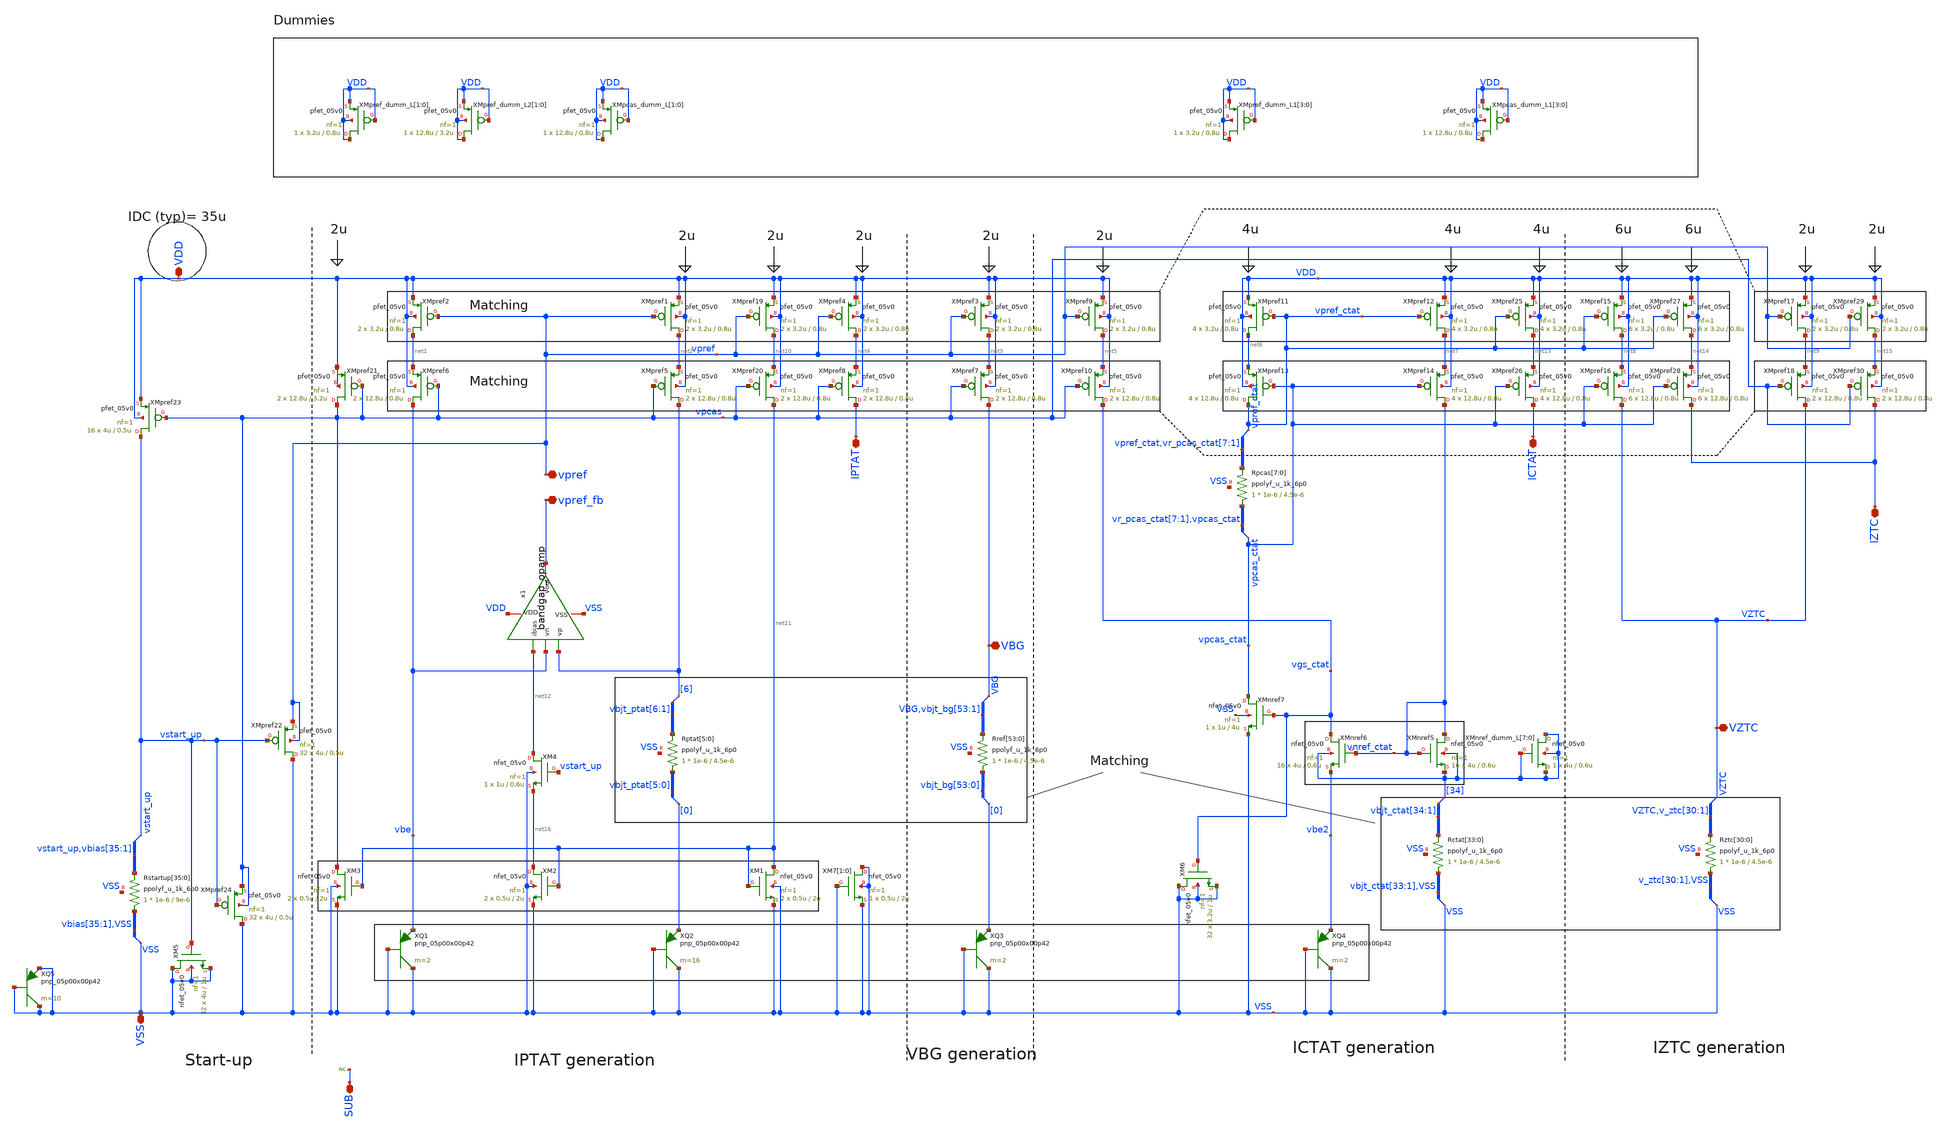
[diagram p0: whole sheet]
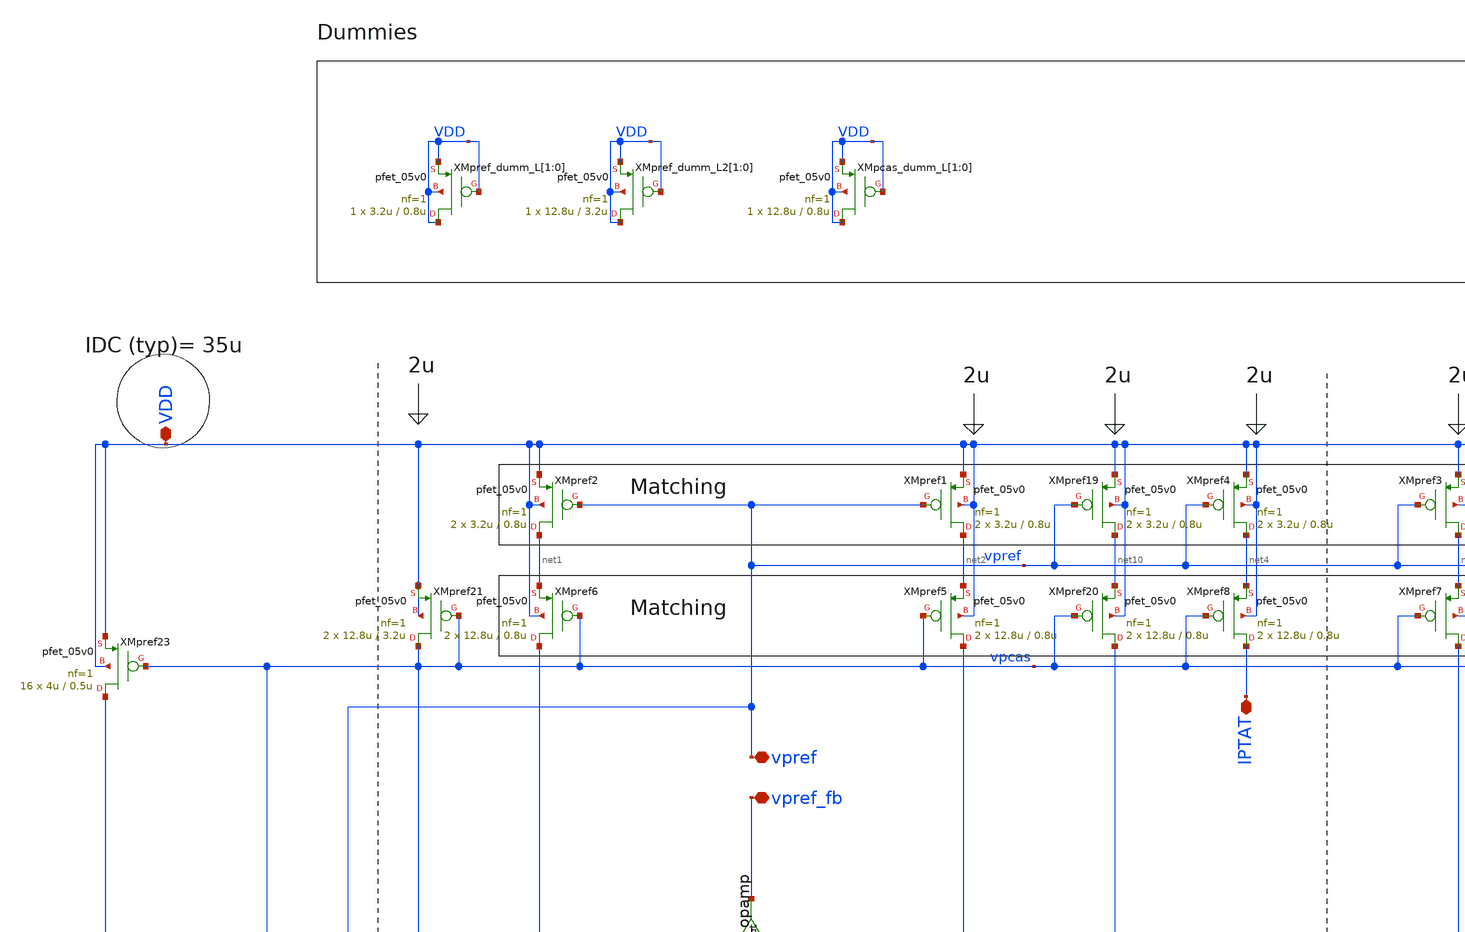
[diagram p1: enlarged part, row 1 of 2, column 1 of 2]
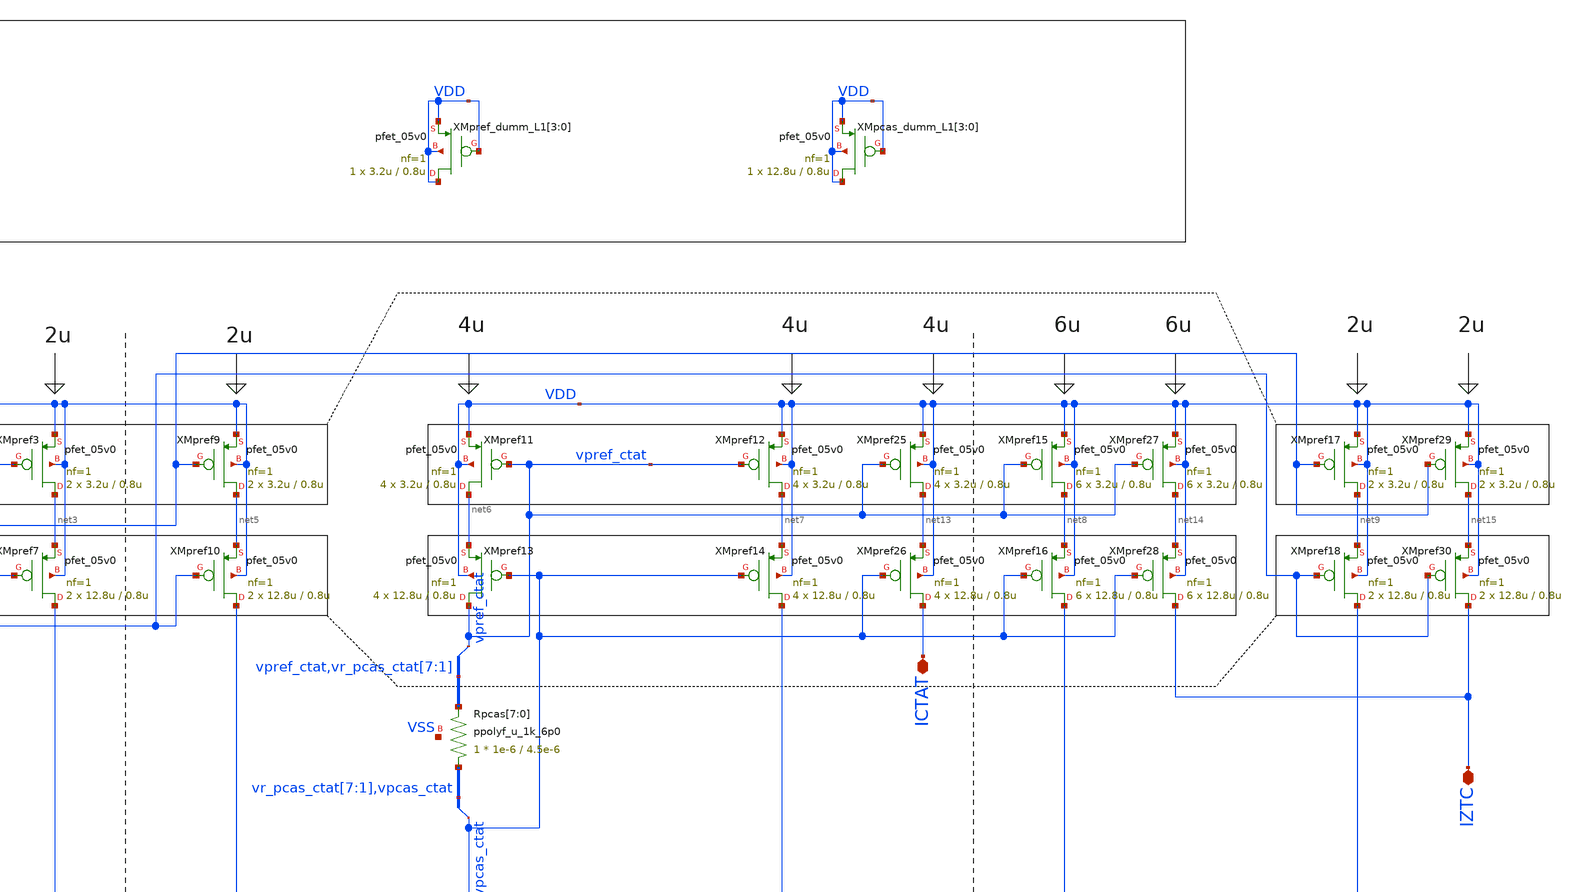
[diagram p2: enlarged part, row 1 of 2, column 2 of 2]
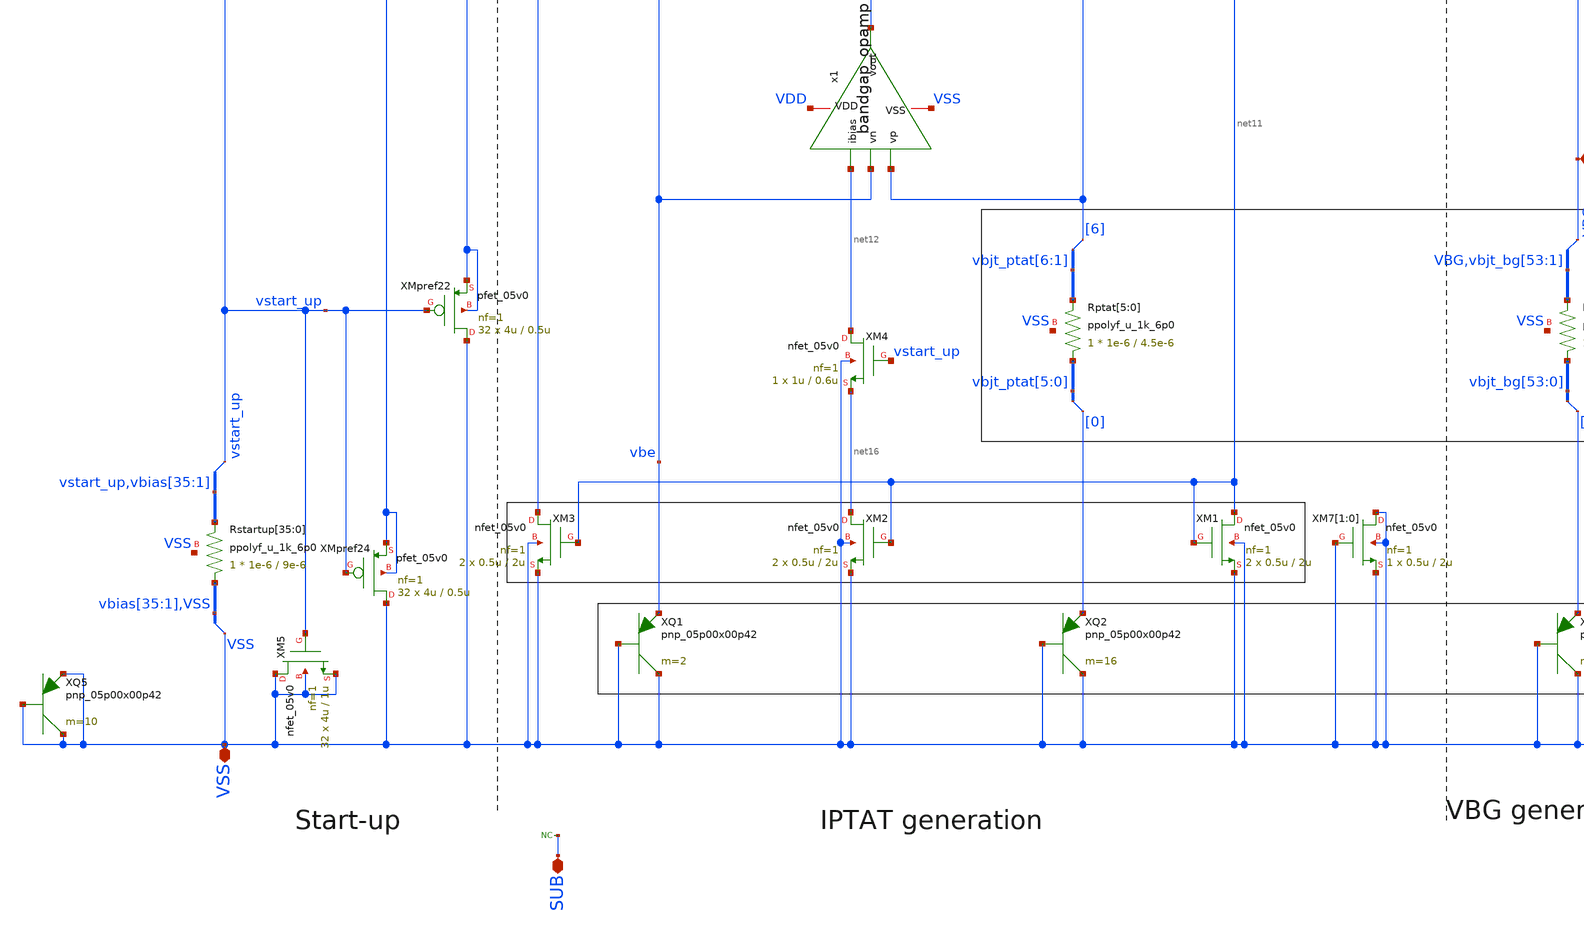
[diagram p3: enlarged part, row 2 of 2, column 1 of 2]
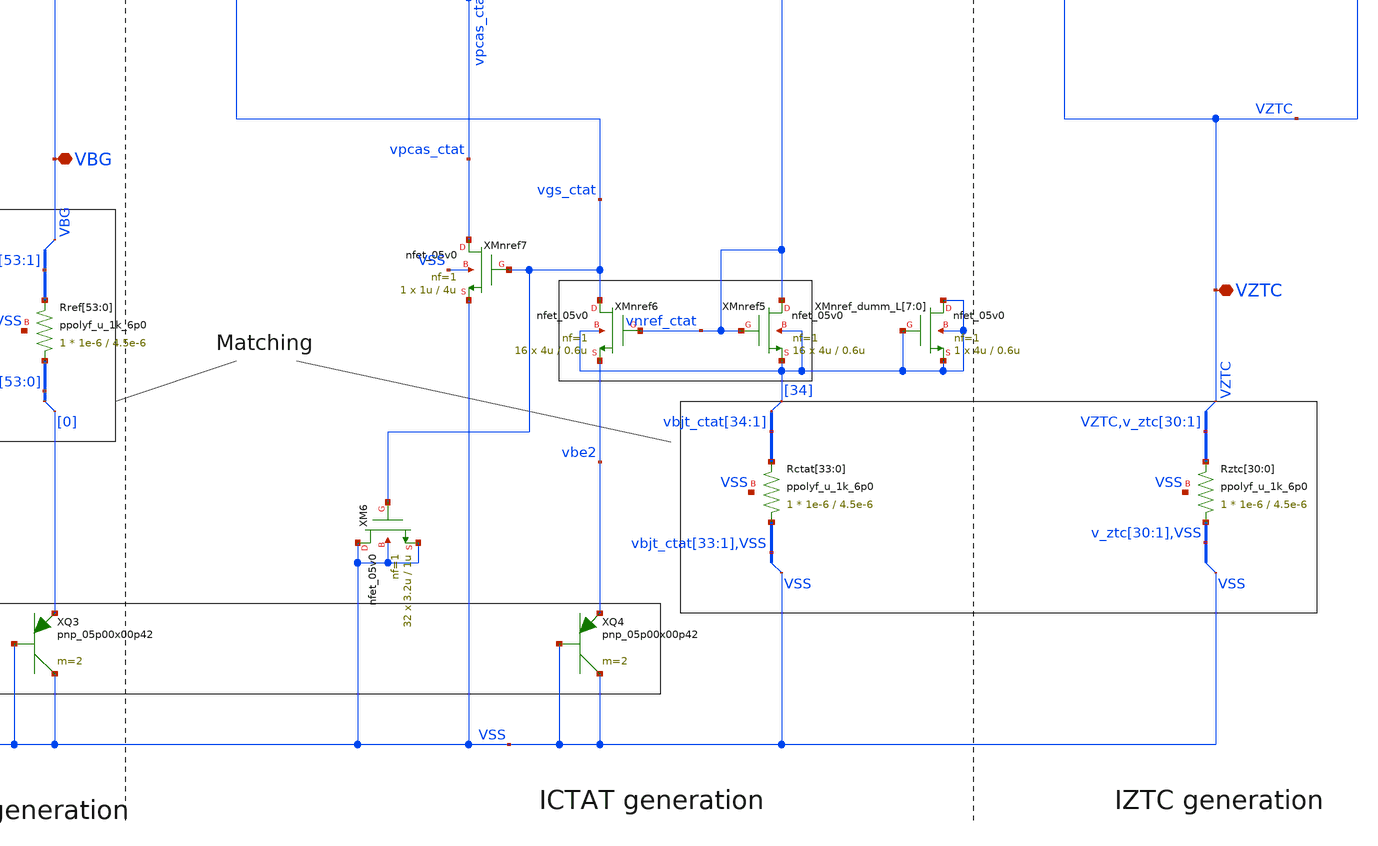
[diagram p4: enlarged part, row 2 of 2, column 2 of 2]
** sch_path: designs/libs/core_bandgap/bandgap/bandgap.sch
**.subckt bandgap VDD VSS SUB VBG IPTAT IZTC vpref vpref_fb ICTAT VZTC
*.iopin VDD
*.iopin VSS
*.iopin SUB
*.iopin VBG
*.iopin IPTAT
*.iopin IZTC
*.iopin vpref
*.iopin vpref_fb
*.iopin ICTAT
*.iopin VZTC
* noconn SUB
XMpref1 net2 vpref VDD VDD pfet_05v0 L=0.8u W=3.2u nf=1 ad='int((nf+1)/2) * W/nf * 0.18u' as='int((nf+2)/2) * W/nf * 0.18u'
+ pd='2*int((nf+1)/2) * (W/nf + 0.18u)' ps='2*int((nf+2)/2) * (W/nf + 0.18u)' nrd='0.18u / W' nrs='0.18u / W'
+ sa=0 sb=0 sd=0 m=2
XMpref2 net1 vpref VDD VDD pfet_05v0 L=0.8u W=3.2u nf=1 ad='int((nf+1)/2) * W/nf * 0.18u' as='int((nf+2)/2) * W/nf * 0.18u'
+ pd='2*int((nf+1)/2) * (W/nf + 0.18u)' ps='2*int((nf+2)/2) * (W/nf + 0.18u)' nrd='0.18u / W' nrs='0.18u / W'
+ sa=0 sb=0 sd=0 m=2
* tap: vbjt_ptat[5:0] --> vbjt_ptat[0]
* tap: vbjt_ptat[6:1] --> vbjt_ptat[6]
XMpref3 net3 vpref VDD VDD pfet_05v0 L=0.8u W=3.2u nf=1 ad='int((nf+1)/2) * W/nf * 0.18u' as='int((nf+2)/2) * W/nf * 0.18u'
+ pd='2*int((nf+1)/2) * (W/nf + 0.18u)' ps='2*int((nf+2)/2) * (W/nf + 0.18u)' nrd='0.18u / W' nrs='0.18u / W'
+ sa=0 sb=0 sd=0 m=2
* tap: vbjt_bg[53:0] --> vbjt_bg[0]
XMpref4 net4 vpref VDD VDD pfet_05v0 L=0.8u W=3.2u nf=1 ad='int((nf+1)/2) * W/nf * 0.18u' as='int((nf+2)/2) * W/nf * 0.18u'
+ pd='2*int((nf+1)/2) * (W/nf + 0.18u)' ps='2*int((nf+2)/2) * (W/nf + 0.18u)' nrd='0.18u / W' nrs='0.18u / W'
+ sa=0 sb=0 sd=0 m=2
XMpref5 vbjt_ptat[6] vpcas net2 VDD pfet_05v0 L=0.8u W=12.8u nf=1 ad='int((nf+1)/2) * W/nf * 0.18u' as='int((nf+2)/2) * W/nf * 0.18u'
+ pd='2*int((nf+1)/2) * (W/nf + 0.18u)' ps='2*int((nf+2)/2) * (W/nf + 0.18u)' nrd='0.18u / W' nrs='0.18u / W'
+ sa=0 sb=0 sd=0 m=2
XMpref6 vbe vpcas net1 VDD pfet_05v0 L=0.8u W=12.8u nf=1 ad='int((nf+1)/2) * W/nf * 0.18u' as='int((nf+2)/2) * W/nf * 0.18u'
+ pd='2*int((nf+1)/2) * (W/nf + 0.18u)' ps='2*int((nf+2)/2) * (W/nf + 0.18u)' nrd='0.18u / W' nrs='0.18u / W'
+ sa=0 sb=0 sd=0 m=2
XMpref7 VBG vpcas net3 VDD pfet_05v0 L=0.8u W=12.8u nf=1 ad='int((nf+1)/2) * W/nf * 0.18u' as='int((nf+2)/2) * W/nf * 0.18u'
+ pd='2*int((nf+1)/2) * (W/nf + 0.18u)' ps='2*int((nf+2)/2) * (W/nf + 0.18u)' nrd='0.18u / W' nrs='0.18u / W'
+ sa=0 sb=0 sd=0 m=2
XMpref8 IPTAT vpcas net4 VDD pfet_05v0 L=0.8u W=12.8u nf=1 ad='int((nf+1)/2) * W/nf * 0.18u' as='int((nf+2)/2) * W/nf * 0.18u'
+ pd='2*int((nf+1)/2) * (W/nf + 0.18u)' ps='2*int((nf+2)/2) * (W/nf + 0.18u)' nrd='0.18u / W' nrs='0.18u / W'
+ sa=0 sb=0 sd=0 m=2
XMnref5 vnref_ctat vnref_ctat vbjt_ctat[34] vbjt_ctat[34] nfet_05v0 L=0.6u W=4u nf=1 ad='int((nf+1)/2) * W/nf * 0.18u'
+ as='int((nf+2)/2) * W/nf * 0.18u' pd='2*int((nf+1)/2) * (W/nf + 0.18u)' ps='2*int((nf+2)/2) * (W/nf + 0.18u)'
+ nrd='0.18u / W' nrs='0.18u / W' sa=0 sb=0 sd=0 m=16
XMnref6 vgs_ctat vnref_ctat vbe2 vbjt_ctat[34] nfet_05v0 L=0.6u W=4u nf=1 ad='int((nf+1)/2) * W/nf * 0.18u'
+ as='int((nf+2)/2) * W/nf * 0.18u' pd='2*int((nf+1)/2) * (W/nf + 0.18u)' ps='2*int((nf+2)/2) * (W/nf + 0.18u)'
+ nrd='0.18u / W' nrs='0.18u / W' sa=0 sb=0 sd=0 m=16
* tap: vbjt_ctat[34:1] --> vbjt_ctat[34]
XMnref7 vpcas_ctat vgs_ctat VSS VSS nfet_05v0 L=4u W=1u nf=1 ad='int((nf+1)/2) * W/nf * 0.18u' as='int((nf+2)/2) * W/nf * 0.18u'
+ pd='2*int((nf+1)/2) * (W/nf + 0.18u)' ps='2*int((nf+2)/2) * (W/nf + 0.18u)' nrd='0.18u / W' nrs='0.18u / W'
+ sa=0 sb=0 sd=0 m=1
XMpref9 net5 vpref VDD VDD pfet_05v0 L=0.8u W=3.2u nf=1 ad='int((nf+1)/2) * W/nf * 0.18u' as='int((nf+2)/2) * W/nf * 0.18u'
+ pd='2*int((nf+1)/2) * (W/nf + 0.18u)' ps='2*int((nf+2)/2) * (W/nf + 0.18u)' nrd='0.18u / W' nrs='0.18u / W'
+ sa=0 sb=0 sd=0 m=2
XMpref10 vgs_ctat vpcas net5 VDD pfet_05v0 L=0.8u W=12.8u nf=1 ad='int((nf+1)/2) * W/nf * 0.18u' as='int((nf+2)/2) * W/nf * 0.18u'
+ pd='2*int((nf+1)/2) * (W/nf + 0.18u)' ps='2*int((nf+2)/2) * (W/nf + 0.18u)' nrd='0.18u / W' nrs='0.18u / W'
+ sa=0 sb=0 sd=0 m=2
XMpref11 net6 vpref_ctat VDD VDD pfet_05v0 L=0.8u W=3.2u nf=1 ad='int((nf+1)/2) * W/nf * 0.18u' as='int((nf+2)/2) * W/nf * 0.18u'
+ pd='2*int((nf+1)/2) * (W/nf + 0.18u)' ps='2*int((nf+2)/2) * (W/nf + 0.18u)' nrd='0.18u / W' nrs='0.18u / W'
+ sa=0 sb=0 sd=0 m=4
XMpref12 net7 vpref_ctat VDD VDD pfet_05v0 L=0.8u W=3.2u nf=1 ad='int((nf+1)/2) * W/nf * 0.18u' as='int((nf+2)/2) * W/nf * 0.18u'
+ pd='2*int((nf+1)/2) * (W/nf + 0.18u)' ps='2*int((nf+2)/2) * (W/nf + 0.18u)' nrd='0.18u / W' nrs='0.18u / W'
+ sa=0 sb=0 sd=0 m=4
XMpref13 vpref_ctat vpcas_ctat net6 VDD pfet_05v0 L=0.8u W=12.8u nf=1 ad='int((nf+1)/2) * W/nf * 0.18u'
+ as='int((nf+2)/2) * W/nf * 0.18u' pd='2*int((nf+1)/2) * (W/nf + 0.18u)' ps='2*int((nf+2)/2) * (W/nf + 0.18u)'
+ nrd='0.18u / W' nrs='0.18u / W' sa=0 sb=0 sd=0 m=4
XMpref14 vnref_ctat vpcas_ctat net7 VDD pfet_05v0 L=0.8u W=12.8u nf=1 ad='int((nf+1)/2) * W/nf * 0.18u'
+ as='int((nf+2)/2) * W/nf * 0.18u' pd='2*int((nf+1)/2) * (W/nf + 0.18u)' ps='2*int((nf+2)/2) * (W/nf + 0.18u)'
+ nrd='0.18u / W' nrs='0.18u / W' sa=0 sb=0 sd=0 m=4
XMpref15 net8 vpref_ctat VDD VDD pfet_05v0 L=0.8u W=3.2u nf=1 ad='int((nf+1)/2) * W/nf * 0.18u' as='int((nf+2)/2) * W/nf * 0.18u'
+ pd='2*int((nf+1)/2) * (W/nf + 0.18u)' ps='2*int((nf+2)/2) * (W/nf + 0.18u)' nrd='0.18u / W' nrs='0.18u / W'
+ sa=0 sb=0 sd=0 m=6
XMpref16 VZTC vpcas_ctat net8 VDD pfet_05v0 L=0.8u W=12.8u nf=1 ad='int((nf+1)/2) * W/nf * 0.18u' as='int((nf+2)/2) * W/nf * 0.18u'
+ pd='2*int((nf+1)/2) * (W/nf + 0.18u)' ps='2*int((nf+2)/2) * (W/nf + 0.18u)' nrd='0.18u / W' nrs='0.18u / W'
+ sa=0 sb=0 sd=0 m=6
XMpref17 net9 vpref VDD VDD pfet_05v0 L=0.8u W=3.2u nf=1 ad='int((nf+1)/2) * W/nf * 0.18u' as='int((nf+2)/2) * W/nf * 0.18u'
+ pd='2*int((nf+1)/2) * (W/nf + 0.18u)' ps='2*int((nf+2)/2) * (W/nf + 0.18u)' nrd='0.18u / W' nrs='0.18u / W'
+ sa=0 sb=0 sd=0 m=2
XMpref18 VZTC vpcas net9 VDD pfet_05v0 L=0.8u W=12.8u nf=1 ad='int((nf+1)/2) * W/nf * 0.18u' as='int((nf+2)/2) * W/nf * 0.18u'
+ pd='2*int((nf+1)/2) * (W/nf + 0.18u)' ps='2*int((nf+2)/2) * (W/nf + 0.18u)' nrd='0.18u / W' nrs='0.18u / W'
+ sa=0 sb=0 sd=0 m=2
XMpref_dumm_L[1] VDD VDD VDD VDD pfet_05v0 L=0.8u W=3.2u nf=1 ad='int((nf+1)/2) * W/nf * 0.18u' as='int((nf+2)/2) * W/nf * 0.18u'
+ pd='2*int((nf+1)/2) * (W/nf + 0.18u)' ps='2*int((nf+2)/2) * (W/nf + 0.18u)' nrd='0.18u / W' nrs='0.18u / W'
+ sa=0 sb=0 sd=0 m=1
XMpref_dumm_L[0] VDD VDD VDD VDD pfet_05v0 L=0.8u W=3.2u nf=1 ad='int((nf+1)/2) * W/nf * 0.18u' as='int((nf+2)/2) * W/nf * 0.18u'
+ pd='2*int((nf+1)/2) * (W/nf + 0.18u)' ps='2*int((nf+2)/2) * (W/nf + 0.18u)' nrd='0.18u / W' nrs='0.18u / W'
+ sa=0 sb=0 sd=0 m=1
x1 VDD net12 vbe vbjt_ptat[6] vpref_fb VSS bandgap_opamp
XMpref19 net10 vpref VDD VDD pfet_05v0 L=0.8u W=3.2u nf=1 ad='int((nf+1)/2) * W/nf * 0.18u' as='int((nf+2)/2) * W/nf * 0.18u'
+ pd='2*int((nf+1)/2) * (W/nf + 0.18u)' ps='2*int((nf+2)/2) * (W/nf + 0.18u)' nrd='0.18u / W' nrs='0.18u / W'
+ sa=0 sb=0 sd=0 m=2
XMpref20 net11 vpcas net10 VDD pfet_05v0 L=0.8u W=12.8u nf=1 ad='int((nf+1)/2) * W/nf * 0.18u' as='int((nf+2)/2) * W/nf * 0.18u'
+ pd='2*int((nf+1)/2) * (W/nf + 0.18u)' ps='2*int((nf+2)/2) * (W/nf + 0.18u)' nrd='0.18u / W' nrs='0.18u / W'
+ sa=0 sb=0 sd=0 m=2
XM1 net11 net11 VSS VSS nfet_05v0 L=2u W=0.5u nf=1 ad='int((nf+1)/2) * W/nf * 0.18u' as='int((nf+2)/2) * W/nf * 0.18u'
+ pd='2*int((nf+1)/2) * (W/nf + 0.18u)' ps='2*int((nf+2)/2) * (W/nf + 0.18u)' nrd='0.18u / W' nrs='0.18u / W'
+ sa=0 sb=0 sd=0 m=2
XM2 net16 net11 VSS VSS nfet_05v0 L=2u W=0.5u nf=1 ad='int((nf+1)/2) * W/nf * 0.18u' as='int((nf+2)/2) * W/nf * 0.18u'
+ pd='2*int((nf+1)/2) * (W/nf + 0.18u)' ps='2*int((nf+2)/2) * (W/nf + 0.18u)' nrd='0.18u / W' nrs='0.18u / W'
+ sa=0 sb=0 sd=0 m=2
XM3 vpcas net11 VSS VSS nfet_05v0 L=2u W=0.5u nf=1 ad='int((nf+1)/2) * W/nf * 0.18u' as='int((nf+2)/2) * W/nf * 0.18u'
+ pd='2*int((nf+1)/2) * (W/nf + 0.18u)' ps='2*int((nf+2)/2) * (W/nf + 0.18u)' nrd='0.18u / W' nrs='0.18u / W'
+ sa=0 sb=0 sd=0 m=2
XMpref21 vpcas vpcas VDD VDD pfet_05v0 L=3.2u W=12.8u nf=1 ad='int((nf+1)/2) * W/nf * 0.18u' as='int((nf+2)/2) * W/nf * 0.18u'
+ pd='2*int((nf+1)/2) * (W/nf + 0.18u)' ps='2*int((nf+2)/2) * (W/nf + 0.18u)' nrd='0.18u / W' nrs='0.18u / W'
+ sa=0 sb=0 sd=0 m=2
XMpref23 vstart_up vpcas VDD VDD pfet_05v0 L=0.5u W=4u nf=1 ad='int((nf+1)/2) * W/nf * 0.18u' as='int((nf+2)/2) * W/nf * 0.18u'
+ pd='2*int((nf+1)/2) * (W/nf + 0.18u)' ps='2*int((nf+2)/2) * (W/nf + 0.18u)' nrd='0.18u / W' nrs='0.18u / W'
+ sa=0 sb=0 sd=0 m=16
XMpref24 VSS vstart_up vpcas vpcas pfet_05v0 L=0.5u W=4u nf=1 ad='int((nf+1)/2) * W/nf * 0.18u' as='int((nf+2)/2) * W/nf * 0.18u'
+ pd='2*int((nf+1)/2) * (W/nf + 0.18u)' ps='2*int((nf+2)/2) * (W/nf + 0.18u)' nrd='0.18u / W' nrs='0.18u / W'
+ sa=0 sb=0 sd=0 m=32
XMpref25 net13 vpref_ctat VDD VDD pfet_05v0 L=0.8u W=3.2u nf=1 ad='int((nf+1)/2) * W/nf * 0.18u' as='int((nf+2)/2) * W/nf * 0.18u'
+ pd='2*int((nf+1)/2) * (W/nf + 0.18u)' ps='2*int((nf+2)/2) * (W/nf + 0.18u)' nrd='0.18u / W' nrs='0.18u / W'
+ sa=0 sb=0 sd=0 m=4
XMpref26 ICTAT vpcas_ctat net13 VDD pfet_05v0 L=0.8u W=12.8u nf=1 ad='int((nf+1)/2) * W/nf * 0.18u' as='int((nf+2)/2) * W/nf * 0.18u'
+ pd='2*int((nf+1)/2) * (W/nf + 0.18u)' ps='2*int((nf+2)/2) * (W/nf + 0.18u)' nrd='0.18u / W' nrs='0.18u / W'
+ sa=0 sb=0 sd=0 m=4
XMpref27 net14 vpref_ctat VDD VDD pfet_05v0 L=0.8u W=3.2u nf=1 ad='int((nf+1)/2) * W/nf * 0.18u' as='int((nf+2)/2) * W/nf * 0.18u'
+ pd='2*int((nf+1)/2) * (W/nf + 0.18u)' ps='2*int((nf+2)/2) * (W/nf + 0.18u)' nrd='0.18u / W' nrs='0.18u / W'
+ sa=0 sb=0 sd=0 m=6
XMpref28 IZTC vpcas_ctat net14 VDD pfet_05v0 L=0.8u W=12.8u nf=1 ad='int((nf+1)/2) * W/nf * 0.18u' as='int((nf+2)/2) * W/nf * 0.18u'
+ pd='2*int((nf+1)/2) * (W/nf + 0.18u)' ps='2*int((nf+2)/2) * (W/nf + 0.18u)' nrd='0.18u / W' nrs='0.18u / W'
+ sa=0 sb=0 sd=0 m=6
XMpref29 net15 vpref VDD VDD pfet_05v0 L=0.8u W=3.2u nf=1 ad='int((nf+1)/2) * W/nf * 0.18u' as='int((nf+2)/2) * W/nf * 0.18u'
+ pd='2*int((nf+1)/2) * (W/nf + 0.18u)' ps='2*int((nf+2)/2) * (W/nf + 0.18u)' nrd='0.18u / W' nrs='0.18u / W'
+ sa=0 sb=0 sd=0 m=2
XMpref30 IZTC vpcas net15 VDD pfet_05v0 L=0.8u W=12.8u nf=1 ad='int((nf+1)/2) * W/nf * 0.18u' as='int((nf+2)/2) * W/nf * 0.18u'
+ pd='2*int((nf+1)/2) * (W/nf + 0.18u)' ps='2*int((nf+2)/2) * (W/nf + 0.18u)' nrd='0.18u / W' nrs='0.18u / W'
+ sa=0 sb=0 sd=0 m=2
XM5 VSS vstart_up VSS VSS nfet_05v0 L=1u W=4u nf=1 ad='int((nf+1)/2) * W/nf * 0.18u' as='int((nf+2)/2) * W/nf * 0.18u'
+ pd='2*int((nf+1)/2) * (W/nf + 0.18u)' ps='2*int((nf+2)/2) * (W/nf + 0.18u)' nrd='0.18u / W' nrs='0.18u / W'
+ sa=0 sb=0 sd=0 m=32
XM4 net12 vstart_up net16 VSS nfet_05v0 L=0.6u W=1u nf=1 ad='int((nf+1)/2) * W/nf * 0.18u' as='int((nf+2)/2) * W/nf * 0.18u'
+ pd='2*int((nf+1)/2) * (W/nf + 0.18u)' ps='2*int((nf+2)/2) * (W/nf + 0.18u)' nrd='0.18u / W' nrs='0.18u / W'
+ sa=0 sb=0 sd=0 m=1
XMpref22 VSS vstart_up vpref vpref pfet_05v0 L=0.5u W=4u nf=1 ad='int((nf+1)/2) * W/nf * 0.18u' as='int((nf+2)/2) * W/nf * 0.18u'
+ pd='2*int((nf+1)/2) * (W/nf + 0.18u)' ps='2*int((nf+2)/2) * (W/nf + 0.18u)' nrd='0.18u / W' nrs='0.18u / W'
+ sa=0 sb=0 sd=0 m=32
XM6 VSS vgs_ctat VSS VSS nfet_05v0 L=1u W=3.2u nf=1 ad='int((nf+1)/2) * W/nf * 0.18u' as='int((nf+2)/2) * W/nf * 0.18u'
+ pd='2*int((nf+1)/2) * (W/nf + 0.18u)' ps='2*int((nf+2)/2) * (W/nf + 0.18u)' nrd='0.18u / W' nrs='0.18u / W'
+ sa=0 sb=0 sd=0 m=32
XMpcas_dumm_L[1] VDD VDD VDD VDD pfet_05v0 L=0.8u W=12.8u nf=1 ad='int((nf+1)/2) * W/nf * 0.18u' as='int((nf+2)/2) * W/nf * 0.18u'
+ pd='2*int((nf+1)/2) * (W/nf + 0.18u)' ps='2*int((nf+2)/2) * (W/nf + 0.18u)' nrd='0.18u / W' nrs='0.18u / W'
+ sa=0 sb=0 sd=0 m=1
XMpcas_dumm_L[0] VDD VDD VDD VDD pfet_05v0 L=0.8u W=12.8u nf=1 ad='int((nf+1)/2) * W/nf * 0.18u' as='int((nf+2)/2) * W/nf * 0.18u'
+ pd='2*int((nf+1)/2) * (W/nf + 0.18u)' ps='2*int((nf+2)/2) * (W/nf + 0.18u)' nrd='0.18u / W' nrs='0.18u / W'
+ sa=0 sb=0 sd=0 m=1
XMpref_dumm_L1[3] VDD VDD VDD VDD pfet_05v0 L=0.8u W=3.2u nf=1 ad='int((nf+1)/2) * W/nf * 0.18u' as='int((nf+2)/2) * W/nf * 0.18u'
+ pd='2*int((nf+1)/2) * (W/nf + 0.18u)' ps='2*int((nf+2)/2) * (W/nf + 0.18u)' nrd='0.18u / W' nrs='0.18u / W'
+ sa=0 sb=0 sd=0 m=1
XMpref_dumm_L1[2] VDD VDD VDD VDD pfet_05v0 L=0.8u W=3.2u nf=1 ad='int((nf+1)/2) * W/nf * 0.18u' as='int((nf+2)/2) * W/nf * 0.18u'
+ pd='2*int((nf+1)/2) * (W/nf + 0.18u)' ps='2*int((nf+2)/2) * (W/nf + 0.18u)' nrd='0.18u / W' nrs='0.18u / W'
+ sa=0 sb=0 sd=0 m=1
XMpref_dumm_L1[1] VDD VDD VDD VDD pfet_05v0 L=0.8u W=3.2u nf=1 ad='int((nf+1)/2) * W/nf * 0.18u' as='int((nf+2)/2) * W/nf * 0.18u'
+ pd='2*int((nf+1)/2) * (W/nf + 0.18u)' ps='2*int((nf+2)/2) * (W/nf + 0.18u)' nrd='0.18u / W' nrs='0.18u / W'
+ sa=0 sb=0 sd=0 m=1
XMpref_dumm_L1[0] VDD VDD VDD VDD pfet_05v0 L=0.8u W=3.2u nf=1 ad='int((nf+1)/2) * W/nf * 0.18u' as='int((nf+2)/2) * W/nf * 0.18u'
+ pd='2*int((nf+1)/2) * (W/nf + 0.18u)' ps='2*int((nf+2)/2) * (W/nf + 0.18u)' nrd='0.18u / W' nrs='0.18u / W'
+ sa=0 sb=0 sd=0 m=1
XMpcas_dumm_L1[3] VDD VDD VDD VDD pfet_05v0 L=0.8u W=12.8u nf=1 ad='int((nf+1)/2) * W/nf * 0.18u' as='int((nf+2)/2) * W/nf * 0.18u'
+ pd='2*int((nf+1)/2) * (W/nf + 0.18u)' ps='2*int((nf+2)/2) * (W/nf + 0.18u)' nrd='0.18u / W' nrs='0.18u / W'
+ sa=0 sb=0 sd=0 m=1
XMpcas_dumm_L1[2] VDD VDD VDD VDD pfet_05v0 L=0.8u W=12.8u nf=1 ad='int((nf+1)/2) * W/nf * 0.18u' as='int((nf+2)/2) * W/nf * 0.18u'
+ pd='2*int((nf+1)/2) * (W/nf + 0.18u)' ps='2*int((nf+2)/2) * (W/nf + 0.18u)' nrd='0.18u / W' nrs='0.18u / W'
+ sa=0 sb=0 sd=0 m=1
XMpcas_dumm_L1[1] VDD VDD VDD VDD pfet_05v0 L=0.8u W=12.8u nf=1 ad='int((nf+1)/2) * W/nf * 0.18u' as='int((nf+2)/2) * W/nf * 0.18u'
+ pd='2*int((nf+1)/2) * (W/nf + 0.18u)' ps='2*int((nf+2)/2) * (W/nf + 0.18u)' nrd='0.18u / W' nrs='0.18u / W'
+ sa=0 sb=0 sd=0 m=1
XMpcas_dumm_L1[0] VDD VDD VDD VDD pfet_05v0 L=0.8u W=12.8u nf=1 ad='int((nf+1)/2) * W/nf * 0.18u' as='int((nf+2)/2) * W/nf * 0.18u'
+ pd='2*int((nf+1)/2) * (W/nf + 0.18u)' ps='2*int((nf+2)/2) * (W/nf + 0.18u)' nrd='0.18u / W' nrs='0.18u / W'
+ sa=0 sb=0 sd=0 m=1
XMpref_dumm_L2[1] VDD VDD VDD VDD pfet_05v0 L=3.2u W=12.8u nf=1 ad='int((nf+1)/2) * W/nf * 0.18u' as='int((nf+2)/2) * W/nf * 0.18u'
+ pd='2*int((nf+1)/2) * (W/nf + 0.18u)' ps='2*int((nf+2)/2) * (W/nf + 0.18u)' nrd='0.18u / W' nrs='0.18u / W'
+ sa=0 sb=0 sd=0 m=1
XMpref_dumm_L2[0] VDD VDD VDD VDD pfet_05v0 L=3.2u W=12.8u nf=1 ad='int((nf+1)/2) * W/nf * 0.18u' as='int((nf+2)/2) * W/nf * 0.18u'
+ pd='2*int((nf+1)/2) * (W/nf + 0.18u)' ps='2*int((nf+2)/2) * (W/nf + 0.18u)' nrd='0.18u / W' nrs='0.18u / W'
+ sa=0 sb=0 sd=0 m=1
XMnref_dumm_L[7] vbjt_ctat[34] vbjt_ctat[34] vbjt_ctat[34] vbjt_ctat[34] nfet_05v0 L=0.6u W=4u nf=1 ad='int((nf+1)/2) * W/nf * 0.18u'
+ as='int((nf+2)/2) * W/nf * 0.18u' pd='2*int((nf+1)/2) * (W/nf + 0.18u)' ps='2*int((nf+2)/2) * (W/nf + 0.18u)'
+ nrd='0.18u / W' nrs='0.18u / W' sa=0 sb=0 sd=0 m=1
XMnref_dumm_L[6] vbjt_ctat[34] vbjt_ctat[34] vbjt_ctat[34] vbjt_ctat[34] nfet_05v0 L=0.6u W=4u nf=1 ad='int((nf+1)/2) * W/nf * 0.18u'
+ as='int((nf+2)/2) * W/nf * 0.18u' pd='2*int((nf+1)/2) * (W/nf + 0.18u)' ps='2*int((nf+2)/2) * (W/nf + 0.18u)'
+ nrd='0.18u / W' nrs='0.18u / W' sa=0 sb=0 sd=0 m=1
XMnref_dumm_L[5] vbjt_ctat[34] vbjt_ctat[34] vbjt_ctat[34] vbjt_ctat[34] nfet_05v0 L=0.6u W=4u nf=1 ad='int((nf+1)/2) * W/nf * 0.18u'
+ as='int((nf+2)/2) * W/nf * 0.18u' pd='2*int((nf+1)/2) * (W/nf + 0.18u)' ps='2*int((nf+2)/2) * (W/nf + 0.18u)'
+ nrd='0.18u / W' nrs='0.18u / W' sa=0 sb=0 sd=0 m=1
XMnref_dumm_L[4] vbjt_ctat[34] vbjt_ctat[34] vbjt_ctat[34] vbjt_ctat[34] nfet_05v0 L=0.6u W=4u nf=1 ad='int((nf+1)/2) * W/nf * 0.18u'
+ as='int((nf+2)/2) * W/nf * 0.18u' pd='2*int((nf+1)/2) * (W/nf + 0.18u)' ps='2*int((nf+2)/2) * (W/nf + 0.18u)'
+ nrd='0.18u / W' nrs='0.18u / W' sa=0 sb=0 sd=0 m=1
XMnref_dumm_L[3] vbjt_ctat[34] vbjt_ctat[34] vbjt_ctat[34] vbjt_ctat[34] nfet_05v0 L=0.6u W=4u nf=1 ad='int((nf+1)/2) * W/nf * 0.18u'
+ as='int((nf+2)/2) * W/nf * 0.18u' pd='2*int((nf+1)/2) * (W/nf + 0.18u)' ps='2*int((nf+2)/2) * (W/nf + 0.18u)'
+ nrd='0.18u / W' nrs='0.18u / W' sa=0 sb=0 sd=0 m=1
XMnref_dumm_L[2] vbjt_ctat[34] vbjt_ctat[34] vbjt_ctat[34] vbjt_ctat[34] nfet_05v0 L=0.6u W=4u nf=1 ad='int((nf+1)/2) * W/nf * 0.18u'
+ as='int((nf+2)/2) * W/nf * 0.18u' pd='2*int((nf+1)/2) * (W/nf + 0.18u)' ps='2*int((nf+2)/2) * (W/nf + 0.18u)'
+ nrd='0.18u / W' nrs='0.18u / W' sa=0 sb=0 sd=0 m=1
XMnref_dumm_L[1] vbjt_ctat[34] vbjt_ctat[34] vbjt_ctat[34] vbjt_ctat[34] nfet_05v0 L=0.6u W=4u nf=1 ad='int((nf+1)/2) * W/nf * 0.18u'
+ as='int((nf+2)/2) * W/nf * 0.18u' pd='2*int((nf+1)/2) * (W/nf + 0.18u)' ps='2*int((nf+2)/2) * (W/nf + 0.18u)'
+ nrd='0.18u / W' nrs='0.18u / W' sa=0 sb=0 sd=0 m=1
XMnref_dumm_L[0] vbjt_ctat[34] vbjt_ctat[34] vbjt_ctat[34] vbjt_ctat[34] nfet_05v0 L=0.6u W=4u nf=1 ad='int((nf+1)/2) * W/nf * 0.18u'
+ as='int((nf+2)/2) * W/nf * 0.18u' pd='2*int((nf+1)/2) * (W/nf + 0.18u)' ps='2*int((nf+2)/2) * (W/nf + 0.18u)'
+ nrd='0.18u / W' nrs='0.18u / W' sa=0 sb=0 sd=0 m=1
XM7[1] VSS VSS VSS VSS nfet_05v0 L=2u W=0.5u nf=1 ad='int((nf+1)/2) * W/nf * 0.18u' as='int((nf+2)/2) * W/nf * 0.18u'
+ pd='2*int((nf+1)/2) * (W/nf + 0.18u)' ps='2*int((nf+2)/2) * (W/nf + 0.18u)' nrd='0.18u / W' nrs='0.18u / W'
+ sa=0 sb=0 sd=0 m=1
XM7[0] VSS VSS VSS VSS nfet_05v0 L=2u W=0.5u nf=1 ad='int((nf+1)/2) * W/nf * 0.18u' as='int((nf+2)/2) * W/nf * 0.18u'
+ pd='2*int((nf+1)/2) * (W/nf + 0.18u)' ps='2*int((nf+2)/2) * (W/nf + 0.18u)' nrd='0.18u / W' nrs='0.18u / W'
+ sa=0 sb=0 sd=0 m=1
XQ1 VSS VSS vbe pnp_05p00x00p42 m=2 par=2
XQ2 VSS VSS vbjt_ptat[0] pnp_05p00x00p42 m=16 par=16
XQ3 VSS VSS vbjt_bg[0] pnp_05p00x00p42 m=2 par=2
XQ4 VSS VSS vbe2 pnp_05p00x00p42 m=2 par=2
XQ5 VSS VSS VSS pnp_05p00x00p42 m=10 par=10
XRstartup[35] vbias[35] vstart_up VSS ppolyf_u_1k_6p0 r_width=1e-6 r_length=9e-6 m=1
XRstartup[34] vbias[34] vbias[35] VSS ppolyf_u_1k_6p0 r_width=1e-6 r_length=9e-6 m=1
XRstartup[33] vbias[33] vbias[34] VSS ppolyf_u_1k_6p0 r_width=1e-6 r_length=9e-6 m=1
XRstartup[32] vbias[32] vbias[33] VSS ppolyf_u_1k_6p0 r_width=1e-6 r_length=9e-6 m=1
XRstartup[31] vbias[31] vbias[32] VSS ppolyf_u_1k_6p0 r_width=1e-6 r_length=9e-6 m=1
XRstartup[30] vbias[30] vbias[31] VSS ppolyf_u_1k_6p0 r_width=1e-6 r_length=9e-6 m=1
XRstartup[29] vbias[29] vbias[30] VSS ppolyf_u_1k_6p0 r_width=1e-6 r_length=9e-6 m=1
XRstartup[28] vbias[28] vbias[29] VSS ppolyf_u_1k_6p0 r_width=1e-6 r_length=9e-6 m=1
XRstartup[27] vbias[27] vbias[28] VSS ppolyf_u_1k_6p0 r_width=1e-6 r_length=9e-6 m=1
XRstartup[26] vbias[26] vbias[27] VSS ppolyf_u_1k_6p0 r_width=1e-6 r_length=9e-6 m=1
XRstartup[25] vbias[25] vbias[26] VSS ppolyf_u_1k_6p0 r_width=1e-6 r_length=9e-6 m=1
XRstartup[24] vbias[24] vbias[25] VSS ppolyf_u_1k_6p0 r_width=1e-6 r_length=9e-6 m=1
XRstartup[23] vbias[23] vbias[24] VSS ppolyf_u_1k_6p0 r_width=1e-6 r_length=9e-6 m=1
XRstartup[22] vbias[22] vbias[23] VSS ppolyf_u_1k_6p0 r_width=1e-6 r_length=9e-6 m=1
XRstartup[21] vbias[21] vbias[22] VSS ppolyf_u_1k_6p0 r_width=1e-6 r_length=9e-6 m=1
XRstartup[20] vbias[20] vbias[21] VSS ppolyf_u_1k_6p0 r_width=1e-6 r_length=9e-6 m=1
XRstartup[19] vbias[19] vbias[20] VSS ppolyf_u_1k_6p0 r_width=1e-6 r_length=9e-6 m=1
XRstartup[18] vbias[18] vbias[19] VSS ppolyf_u_1k_6p0 r_width=1e-6 r_length=9e-6 m=1
XRstartup[17] vbias[17] vbias[18] VSS ppolyf_u_1k_6p0 r_width=1e-6 r_length=9e-6 m=1
XRstartup[16] vbias[16] vbias[17] VSS ppolyf_u_1k_6p0 r_width=1e-6 r_length=9e-6 m=1
XRstartup[15] vbias[15] vbias[16] VSS ppolyf_u_1k_6p0 r_width=1e-6 r_length=9e-6 m=1
XRstartup[14] vbias[14] vbias[15] VSS ppolyf_u_1k_6p0 r_width=1e-6 r_length=9e-6 m=1
XRstartup[13] vbias[13] vbias[14] VSS ppolyf_u_1k_6p0 r_width=1e-6 r_length=9e-6 m=1
XRstartup[12] vbias[12] vbias[13] VSS ppolyf_u_1k_6p0 r_width=1e-6 r_length=9e-6 m=1
XRstartup[11] vbias[11] vbias[12] VSS ppolyf_u_1k_6p0 r_width=1e-6 r_length=9e-6 m=1
XRstartup[10] vbias[10] vbias[11] VSS ppolyf_u_1k_6p0 r_width=1e-6 r_length=9e-6 m=1
XRstartup[9] vbias[9] vbias[10] VSS ppolyf_u_1k_6p0 r_width=1e-6 r_length=9e-6 m=1
XRstartup[8] vbias[8] vbias[9] VSS ppolyf_u_1k_6p0 r_width=1e-6 r_length=9e-6 m=1
XRstartup[7] vbias[7] vbias[8] VSS ppolyf_u_1k_6p0 r_width=1e-6 r_length=9e-6 m=1
XRstartup[6] vbias[6] vbias[7] VSS ppolyf_u_1k_6p0 r_width=1e-6 r_length=9e-6 m=1
XRstartup[5] vbias[5] vbias[6] VSS ppolyf_u_1k_6p0 r_width=1e-6 r_length=9e-6 m=1
XRstartup[4] vbias[4] vbias[5] VSS ppolyf_u_1k_6p0 r_width=1e-6 r_length=9e-6 m=1
XRstartup[3] vbias[3] vbias[4] VSS ppolyf_u_1k_6p0 r_width=1e-6 r_length=9e-6 m=1
XRstartup[2] vbias[2] vbias[3] VSS ppolyf_u_1k_6p0 r_width=1e-6 r_length=9e-6 m=1
XRstartup[1] vbias[1] vbias[2] VSS ppolyf_u_1k_6p0 r_width=1e-6 r_length=9e-6 m=1
XRstartup[0] VSS vbias[1] VSS ppolyf_u_1k_6p0 r_width=1e-6 r_length=9e-6 m=1
XRptat[5] vbjt_ptat[5] vbjt_ptat[6] VSS ppolyf_u_1k_6p0 r_width=1e-6 r_length=4.5e-6 m=1
XRptat[4] vbjt_ptat[4] vbjt_ptat[5] VSS ppolyf_u_1k_6p0 r_width=1e-6 r_length=4.5e-6 m=1
XRptat[3] vbjt_ptat[3] vbjt_ptat[4] VSS ppolyf_u_1k_6p0 r_width=1e-6 r_length=4.5e-6 m=1
XRptat[2] vbjt_ptat[2] vbjt_ptat[3] VSS ppolyf_u_1k_6p0 r_width=1e-6 r_length=4.5e-6 m=1
XRptat[1] vbjt_ptat[1] vbjt_ptat[2] VSS ppolyf_u_1k_6p0 r_width=1e-6 r_length=4.5e-6 m=1
XRptat[0] vbjt_ptat[0] vbjt_ptat[1] VSS ppolyf_u_1k_6p0 r_width=1e-6 r_length=4.5e-6 m=1
XRref[53] vbjt_bg[53] VBG VSS ppolyf_u_1k_6p0 r_width=1e-6 r_length=4.5e-6 m=1
XRref[52] vbjt_bg[52] vbjt_bg[53] VSS ppolyf_u_1k_6p0 r_width=1e-6 r_length=4.5e-6 m=1
XRref[51] vbjt_bg[51] vbjt_bg[52] VSS ppolyf_u_1k_6p0 r_width=1e-6 r_length=4.5e-6 m=1
XRref[50] vbjt_bg[50] vbjt_bg[51] VSS ppolyf_u_1k_6p0 r_width=1e-6 r_length=4.5e-6 m=1
XRref[49] vbjt_bg[49] vbjt_bg[50] VSS ppolyf_u_1k_6p0 r_width=1e-6 r_length=4.5e-6 m=1
XRref[48] vbjt_bg[48] vbjt_bg[49] VSS ppolyf_u_1k_6p0 r_width=1e-6 r_length=4.5e-6 m=1
XRref[47] vbjt_bg[47] vbjt_bg[48] VSS ppolyf_u_1k_6p0 r_width=1e-6 r_length=4.5e-6 m=1
XRref[46] vbjt_bg[46] vbjt_bg[47] VSS ppolyf_u_1k_6p0 r_width=1e-6 r_length=4.5e-6 m=1
XRref[45] vbjt_bg[45] vbjt_bg[46] VSS ppolyf_u_1k_6p0 r_width=1e-6 r_length=4.5e-6 m=1
XRref[44] vbjt_bg[44] vbjt_bg[45] VSS ppolyf_u_1k_6p0 r_width=1e-6 r_length=4.5e-6 m=1
XRref[43] vbjt_bg[43] vbjt_bg[44] VSS ppolyf_u_1k_6p0 r_width=1e-6 r_length=4.5e-6 m=1
XRref[42] vbjt_bg[42] vbjt_bg[43] VSS ppolyf_u_1k_6p0 r_width=1e-6 r_length=4.5e-6 m=1
XRref[41] vbjt_bg[41] vbjt_bg[42] VSS ppolyf_u_1k_6p0 r_width=1e-6 r_length=4.5e-6 m=1
XRref[40] vbjt_bg[40] vbjt_bg[41] VSS ppolyf_u_1k_6p0 r_width=1e-6 r_length=4.5e-6 m=1
XRref[39] vbjt_bg[39] vbjt_bg[40] VSS ppolyf_u_1k_6p0 r_width=1e-6 r_length=4.5e-6 m=1
XRref[38] vbjt_bg[38] vbjt_bg[39] VSS ppolyf_u_1k_6p0 r_width=1e-6 r_length=4.5e-6 m=1
XRref[37] vbjt_bg[37] vbjt_bg[38] VSS ppolyf_u_1k_6p0 r_width=1e-6 r_length=4.5e-6 m=1
XRref[36] vbjt_bg[36] vbjt_bg[37] VSS ppolyf_u_1k_6p0 r_width=1e-6 r_length=4.5e-6 m=1
XRref[35] vbjt_bg[35] vbjt_bg[36] VSS ppolyf_u_1k_6p0 r_width=1e-6 r_length=4.5e-6 m=1
XRref[34] vbjt_bg[34] vbjt_bg[35] VSS ppolyf_u_1k_6p0 r_width=1e-6 r_length=4.5e-6 m=1
XRref[33] vbjt_bg[33] vbjt_bg[34] VSS ppolyf_u_1k_6p0 r_width=1e-6 r_length=4.5e-6 m=1
XRref[32] vbjt_bg[32] vbjt_bg[33] VSS ppolyf_u_1k_6p0 r_width=1e-6 r_length=4.5e-6 m=1
XRref[31] vbjt_bg[31] vbjt_bg[32] VSS ppolyf_u_1k_6p0 r_width=1e-6 r_length=4.5e-6 m=1
XRref[30] vbjt_bg[30] vbjt_bg[31] VSS ppolyf_u_1k_6p0 r_width=1e-6 r_length=4.5e-6 m=1
XRref[29] vbjt_bg[29] vbjt_bg[30] VSS ppolyf_u_1k_6p0 r_width=1e-6 r_length=4.5e-6 m=1
XRref[28] vbjt_bg[28] vbjt_bg[29] VSS ppolyf_u_1k_6p0 r_width=1e-6 r_length=4.5e-6 m=1
XRref[27] vbjt_bg[27] vbjt_bg[28] VSS ppolyf_u_1k_6p0 r_width=1e-6 r_length=4.5e-6 m=1
XRref[26] vbjt_bg[26] vbjt_bg[27] VSS ppolyf_u_1k_6p0 r_width=1e-6 r_length=4.5e-6 m=1
XRref[25] vbjt_bg[25] vbjt_bg[26] VSS ppolyf_u_1k_6p0 r_width=1e-6 r_length=4.5e-6 m=1
XRref[24] vbjt_bg[24] vbjt_bg[25] VSS ppolyf_u_1k_6p0 r_width=1e-6 r_length=4.5e-6 m=1
XRref[23] vbjt_bg[23] vbjt_bg[24] VSS ppolyf_u_1k_6p0 r_width=1e-6 r_length=4.5e-6 m=1
XRref[22] vbjt_bg[22] vbjt_bg[23] VSS ppolyf_u_1k_6p0 r_width=1e-6 r_length=4.5e-6 m=1
XRref[21] vbjt_bg[21] vbjt_bg[22] VSS ppolyf_u_1k_6p0 r_width=1e-6 r_length=4.5e-6 m=1
XRref[20] vbjt_bg[20] vbjt_bg[21] VSS ppolyf_u_1k_6p0 r_width=1e-6 r_length=4.5e-6 m=1
XRref[19] vbjt_bg[19] vbjt_bg[20] VSS ppolyf_u_1k_6p0 r_width=1e-6 r_length=4.5e-6 m=1
XRref[18] vbjt_bg[18] vbjt_bg[19] VSS ppolyf_u_1k_6p0 r_width=1e-6 r_length=4.5e-6 m=1
XRref[17] vbjt_bg[17] vbjt_bg[18] VSS ppolyf_u_1k_6p0 r_width=1e-6 r_length=4.5e-6 m=1
XRref[16] vbjt_bg[16] vbjt_bg[17] VSS ppolyf_u_1k_6p0 r_width=1e-6 r_length=4.5e-6 m=1
XRref[15] vbjt_bg[15] vbjt_bg[16] VSS ppolyf_u_1k_6p0 r_width=1e-6 r_length=4.5e-6 m=1
XRref[14] vbjt_bg[14] vbjt_bg[15] VSS ppolyf_u_1k_6p0 r_width=1e-6 r_length=4.5e-6 m=1
XRref[13] vbjt_bg[13] vbjt_bg[14] VSS ppolyf_u_1k_6p0 r_width=1e-6 r_length=4.5e-6 m=1
XRref[12] vbjt_bg[12] vbjt_bg[13] VSS ppolyf_u_1k_6p0 r_width=1e-6 r_length=4.5e-6 m=1
XRref[11] vbjt_bg[11] vbjt_bg[12] VSS ppolyf_u_1k_6p0 r_width=1e-6 r_length=4.5e-6 m=1
XRref[10] vbjt_bg[10] vbjt_bg[11] VSS ppolyf_u_1k_6p0 r_width=1e-6 r_length=4.5e-6 m=1
XRref[9] vbjt_bg[9] vbjt_bg[10] VSS ppolyf_u_1k_6p0 r_width=1e-6 r_length=4.5e-6 m=1
XRref[8] vbjt_bg[8] vbjt_bg[9] VSS ppolyf_u_1k_6p0 r_width=1e-6 r_length=4.5e-6 m=1
XRref[7] vbjt_bg[7] vbjt_bg[8] VSS ppolyf_u_1k_6p0 r_width=1e-6 r_length=4.5e-6 m=1
XRref[6] vbjt_bg[6] vbjt_bg[7] VSS ppolyf_u_1k_6p0 r_width=1e-6 r_length=4.5e-6 m=1
XRref[5] vbjt_bg[5] vbjt_bg[6] VSS ppolyf_u_1k_6p0 r_width=1e-6 r_length=4.5e-6 m=1
XRref[4] vbjt_bg[4] vbjt_bg[5] VSS ppolyf_u_1k_6p0 r_width=1e-6 r_length=4.5e-6 m=1
XRref[3] vbjt_bg[3] vbjt_bg[4] VSS ppolyf_u_1k_6p0 r_width=1e-6 r_length=4.5e-6 m=1
XRref[2] vbjt_bg[2] vbjt_bg[3] VSS ppolyf_u_1k_6p0 r_width=1e-6 r_length=4.5e-6 m=1
XRref[1] vbjt_bg[1] vbjt_bg[2] VSS ppolyf_u_1k_6p0 r_width=1e-6 r_length=4.5e-6 m=1
XRref[0] vbjt_bg[0] vbjt_bg[1] VSS ppolyf_u_1k_6p0 r_width=1e-6 r_length=4.5e-6 m=1
XRpcas[7] vr_pcas_ctat[7] vpref_ctat VSS ppolyf_u_1k_6p0 r_width=1e-6 r_length=4.5e-6 m=1
XRpcas[6] vr_pcas_ctat[6] vr_pcas_ctat[7] VSS ppolyf_u_1k_6p0 r_width=1e-6 r_length=4.5e-6 m=1
XRpcas[5] vr_pcas_ctat[5] vr_pcas_ctat[6] VSS ppolyf_u_1k_6p0 r_width=1e-6 r_length=4.5e-6 m=1
XRpcas[4] vr_pcas_ctat[4] vr_pcas_ctat[5] VSS ppolyf_u_1k_6p0 r_width=1e-6 r_length=4.5e-6 m=1
XRpcas[3] vr_pcas_ctat[3] vr_pcas_ctat[4] VSS ppolyf_u_1k_6p0 r_width=1e-6 r_length=4.5e-6 m=1
XRpcas[2] vr_pcas_ctat[2] vr_pcas_ctat[3] VSS ppolyf_u_1k_6p0 r_width=1e-6 r_length=4.5e-6 m=1
XRpcas[1] vr_pcas_ctat[1] vr_pcas_ctat[2] VSS ppolyf_u_1k_6p0 r_width=1e-6 r_length=4.5e-6 m=1
XRpcas[0] vpcas_ctat vr_pcas_ctat[1] VSS ppolyf_u_1k_6p0 r_width=1e-6 r_length=4.5e-6 m=1
XRctat[33] vbjt_ctat[33] vbjt_ctat[34] VSS ppolyf_u_1k_6p0 r_width=1e-6 r_length=4.5e-6 m=1
XRctat[32] vbjt_ctat[32] vbjt_ctat[33] VSS ppolyf_u_1k_6p0 r_width=1e-6 r_length=4.5e-6 m=1
XRctat[31] vbjt_ctat[31] vbjt_ctat[32] VSS ppolyf_u_1k_6p0 r_width=1e-6 r_length=4.5e-6 m=1
XRctat[30] vbjt_ctat[30] vbjt_ctat[31] VSS ppolyf_u_1k_6p0 r_width=1e-6 r_length=4.5e-6 m=1
XRctat[29] vbjt_ctat[29] vbjt_ctat[30] VSS ppolyf_u_1k_6p0 r_width=1e-6 r_length=4.5e-6 m=1
XRctat[28] vbjt_ctat[28] vbjt_ctat[29] VSS ppolyf_u_1k_6p0 r_width=1e-6 r_length=4.5e-6 m=1
XRctat[27] vbjt_ctat[27] vbjt_ctat[28] VSS ppolyf_u_1k_6p0 r_width=1e-6 r_length=4.5e-6 m=1
XRctat[26] vbjt_ctat[26] vbjt_ctat[27] VSS ppolyf_u_1k_6p0 r_width=1e-6 r_length=4.5e-6 m=1
XRctat[25] vbjt_ctat[25] vbjt_ctat[26] VSS ppolyf_u_1k_6p0 r_width=1e-6 r_length=4.5e-6 m=1
XRctat[24] vbjt_ctat[24] vbjt_ctat[25] VSS ppolyf_u_1k_6p0 r_width=1e-6 r_length=4.5e-6 m=1
XRctat[23] vbjt_ctat[23] vbjt_ctat[24] VSS ppolyf_u_1k_6p0 r_width=1e-6 r_length=4.5e-6 m=1
XRctat[22] vbjt_ctat[22] vbjt_ctat[23] VSS ppolyf_u_1k_6p0 r_width=1e-6 r_length=4.5e-6 m=1
XRctat[21] vbjt_ctat[21] vbjt_ctat[22] VSS ppolyf_u_1k_6p0 r_width=1e-6 r_length=4.5e-6 m=1
XRctat[20] vbjt_ctat[20] vbjt_ctat[21] VSS ppolyf_u_1k_6p0 r_width=1e-6 r_length=4.5e-6 m=1
XRctat[19] vbjt_ctat[19] vbjt_ctat[20] VSS ppolyf_u_1k_6p0 r_width=1e-6 r_length=4.5e-6 m=1
XRctat[18] vbjt_ctat[18] vbjt_ctat[19] VSS ppolyf_u_1k_6p0 r_width=1e-6 r_length=4.5e-6 m=1
XRctat[17] vbjt_ctat[17] vbjt_ctat[18] VSS ppolyf_u_1k_6p0 r_width=1e-6 r_length=4.5e-6 m=1
XRctat[16] vbjt_ctat[16] vbjt_ctat[17] VSS ppolyf_u_1k_6p0 r_width=1e-6 r_length=4.5e-6 m=1
XRctat[15] vbjt_ctat[15] vbjt_ctat[16] VSS ppolyf_u_1k_6p0 r_width=1e-6 r_length=4.5e-6 m=1
XRctat[14] vbjt_ctat[14] vbjt_ctat[15] VSS ppolyf_u_1k_6p0 r_width=1e-6 r_length=4.5e-6 m=1
XRctat[13] vbjt_ctat[13] vbjt_ctat[14] VSS ppolyf_u_1k_6p0 r_width=1e-6 r_length=4.5e-6 m=1
XRctat[12] vbjt_ctat[12] vbjt_ctat[13] VSS ppolyf_u_1k_6p0 r_width=1e-6 r_length=4.5e-6 m=1
XRctat[11] vbjt_ctat[11] vbjt_ctat[12] VSS ppolyf_u_1k_6p0 r_width=1e-6 r_length=4.5e-6 m=1
XRctat[10] vbjt_ctat[10] vbjt_ctat[11] VSS ppolyf_u_1k_6p0 r_width=1e-6 r_length=4.5e-6 m=1
XRctat[9] vbjt_ctat[9] vbjt_ctat[10] VSS ppolyf_u_1k_6p0 r_width=1e-6 r_length=4.5e-6 m=1
XRctat[8] vbjt_ctat[8] vbjt_ctat[9] VSS ppolyf_u_1k_6p0 r_width=1e-6 r_length=4.5e-6 m=1
XRctat[7] vbjt_ctat[7] vbjt_ctat[8] VSS ppolyf_u_1k_6p0 r_width=1e-6 r_length=4.5e-6 m=1
XRctat[6] vbjt_ctat[6] vbjt_ctat[7] VSS ppolyf_u_1k_6p0 r_width=1e-6 r_length=4.5e-6 m=1
XRctat[5] vbjt_ctat[5] vbjt_ctat[6] VSS ppolyf_u_1k_6p0 r_width=1e-6 r_length=4.5e-6 m=1
XRctat[4] vbjt_ctat[4] vbjt_ctat[5] VSS ppolyf_u_1k_6p0 r_width=1e-6 r_length=4.5e-6 m=1
XRctat[3] vbjt_ctat[3] vbjt_ctat[4] VSS ppolyf_u_1k_6p0 r_width=1e-6 r_length=4.5e-6 m=1
XRctat[2] vbjt_ctat[2] vbjt_ctat[3] VSS ppolyf_u_1k_6p0 r_width=1e-6 r_length=4.5e-6 m=1
XRctat[1] vbjt_ctat[1] vbjt_ctat[2] VSS ppolyf_u_1k_6p0 r_width=1e-6 r_length=4.5e-6 m=1
XRctat[0] VSS vbjt_ctat[1] VSS ppolyf_u_1k_6p0 r_width=1e-6 r_length=4.5e-6 m=1
XRztc[30] v_ztc[30] VZTC VSS ppolyf_u_1k_6p0 r_width=1e-6 r_length=4.5e-6 m=1
XRztc[29] v_ztc[29] v_ztc[30] VSS ppolyf_u_1k_6p0 r_width=1e-6 r_length=4.5e-6 m=1
XRztc[28] v_ztc[28] v_ztc[29] VSS ppolyf_u_1k_6p0 r_width=1e-6 r_length=4.5e-6 m=1
XRztc[27] v_ztc[27] v_ztc[28] VSS ppolyf_u_1k_6p0 r_width=1e-6 r_length=4.5e-6 m=1
XRztc[26] v_ztc[26] v_ztc[27] VSS ppolyf_u_1k_6p0 r_width=1e-6 r_length=4.5e-6 m=1
XRztc[25] v_ztc[25] v_ztc[26] VSS ppolyf_u_1k_6p0 r_width=1e-6 r_length=4.5e-6 m=1
XRztc[24] v_ztc[24] v_ztc[25] VSS ppolyf_u_1k_6p0 r_width=1e-6 r_length=4.5e-6 m=1
XRztc[23] v_ztc[23] v_ztc[24] VSS ppolyf_u_1k_6p0 r_width=1e-6 r_length=4.5e-6 m=1
XRztc[22] v_ztc[22] v_ztc[23] VSS ppolyf_u_1k_6p0 r_width=1e-6 r_length=4.5e-6 m=1
XRztc[21] v_ztc[21] v_ztc[22] VSS ppolyf_u_1k_6p0 r_width=1e-6 r_length=4.5e-6 m=1
XRztc[20] v_ztc[20] v_ztc[21] VSS ppolyf_u_1k_6p0 r_width=1e-6 r_length=4.5e-6 m=1
XRztc[19] v_ztc[19] v_ztc[20] VSS ppolyf_u_1k_6p0 r_width=1e-6 r_length=4.5e-6 m=1
XRztc[18] v_ztc[18] v_ztc[19] VSS ppolyf_u_1k_6p0 r_width=1e-6 r_length=4.5e-6 m=1
XRztc[17] v_ztc[17] v_ztc[18] VSS ppolyf_u_1k_6p0 r_width=1e-6 r_length=4.5e-6 m=1
XRztc[16] v_ztc[16] v_ztc[17] VSS ppolyf_u_1k_6p0 r_width=1e-6 r_length=4.5e-6 m=1
XRztc[15] v_ztc[15] v_ztc[16] VSS ppolyf_u_1k_6p0 r_width=1e-6 r_length=4.5e-6 m=1
XRztc[14] v_ztc[14] v_ztc[15] VSS ppolyf_u_1k_6p0 r_width=1e-6 r_length=4.5e-6 m=1
XRztc[13] v_ztc[13] v_ztc[14] VSS ppolyf_u_1k_6p0 r_width=1e-6 r_length=4.5e-6 m=1
XRztc[12] v_ztc[12] v_ztc[13] VSS ppolyf_u_1k_6p0 r_width=1e-6 r_length=4.5e-6 m=1
XRztc[11] v_ztc[11] v_ztc[12] VSS ppolyf_u_1k_6p0 r_width=1e-6 r_length=4.5e-6 m=1
XRztc[10] v_ztc[10] v_ztc[11] VSS ppolyf_u_1k_6p0 r_width=1e-6 r_length=4.5e-6 m=1
XRztc[9] v_ztc[9] v_ztc[10] VSS ppolyf_u_1k_6p0 r_width=1e-6 r_length=4.5e-6 m=1
XRztc[8] v_ztc[8] v_ztc[9] VSS ppolyf_u_1k_6p0 r_width=1e-6 r_length=4.5e-6 m=1
XRztc[7] v_ztc[7] v_ztc[8] VSS ppolyf_u_1k_6p0 r_width=1e-6 r_length=4.5e-6 m=1
XRztc[6] v_ztc[6] v_ztc[7] VSS ppolyf_u_1k_6p0 r_width=1e-6 r_length=4.5e-6 m=1
XRztc[5] v_ztc[5] v_ztc[6] VSS ppolyf_u_1k_6p0 r_width=1e-6 r_length=4.5e-6 m=1
XRztc[4] v_ztc[4] v_ztc[5] VSS ppolyf_u_1k_6p0 r_width=1e-6 r_length=4.5e-6 m=1
XRztc[3] v_ztc[3] v_ztc[4] VSS ppolyf_u_1k_6p0 r_width=1e-6 r_length=4.5e-6 m=1
XRztc[2] v_ztc[2] v_ztc[3] VSS ppolyf_u_1k_6p0 r_width=1e-6 r_length=4.5e-6 m=1
XRztc[1] v_ztc[1] v_ztc[2] VSS ppolyf_u_1k_6p0 r_width=1e-6 r_length=4.5e-6 m=1
XRztc[0] VSS v_ztc[1] VSS ppolyf_u_1k_6p0 r_width=1e-6 r_length=4.5e-6 m=1
**.ends
.end
